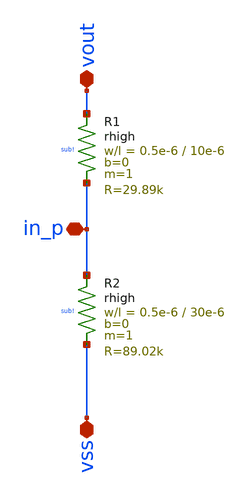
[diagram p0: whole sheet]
** sch_path: AC3E-IHP_ALDO/design_data/klayout/netlist/rdiv.sch
**.subckt rdiv vout vss in_p
*.iopin vout
*.iopin vss
*.iopin in_p
XR2 in_p vss sub! rhigh w=0.5e-6 l=30e-6 m=1 b=0 mm_ok=1
XR1 vout in_p sub! rhigh w=0.5e-6 l=10e-6 m=1 b=0 mm_ok=1
**.ends
.end
